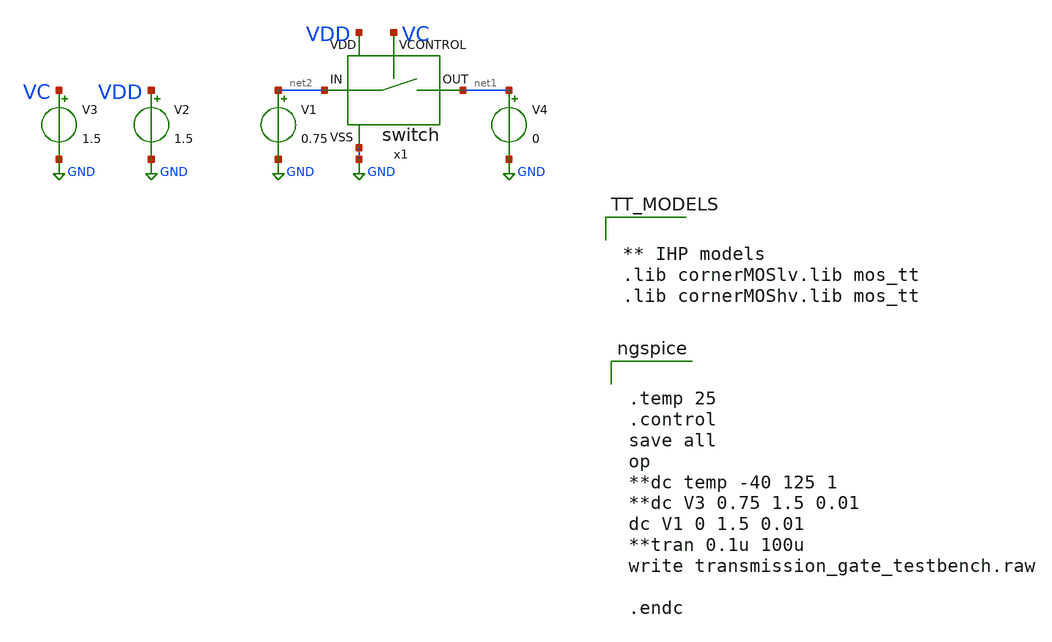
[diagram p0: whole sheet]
** sch_path: 10_xschem/transmission_gate_testbench.sch
**.subckt transmission_gate_testbench
x1 net1 net2 VDD VC GND switch
V1 net2 GND 0.75
V2 VDD GND 1.5
V3 VC GND 1.5
V4 net1 GND 0
**** begin user architecture code


.temp 25
.control
save all
op
**dc temp -40 125 1
**dc V3 0.75 1.5 0.01
dc V1 0 1.5 0.01
**tran 0.1u 100u
write transmission_gate_testbench.raw

.endc




** IHP models
.lib cornerMOSlv.lib mos_tt
.lib cornerMOShv.lib mos_tt


**** end user architecture code
**.ends
.GLOBAL GND
.end
